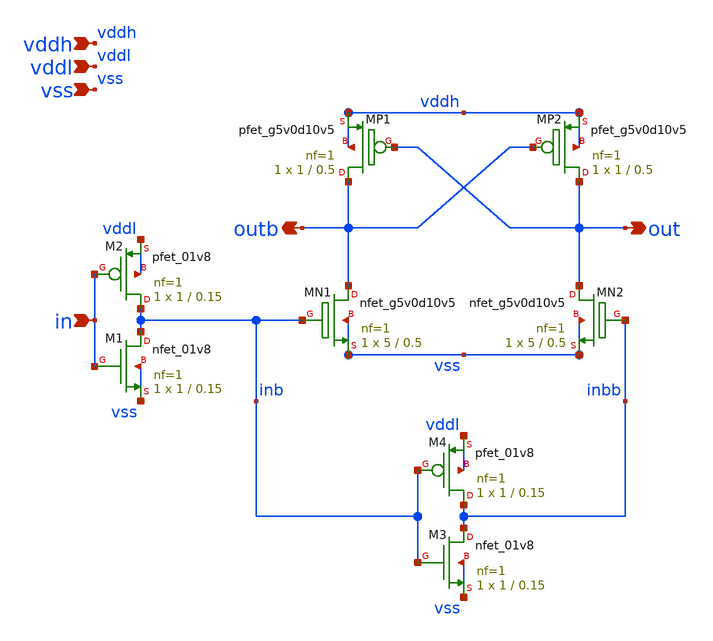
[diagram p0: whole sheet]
** sch_path: level_shifters/ls_conv.sch
**.subckt ls_conv vddh vss vddl in out outb
*.ipin vddh
*.ipin vss
*.ipin vddl
*.ipin in
*.opin out
*.opin outb
XMN1 outb inb vss vss sky130_fd_pr__nfet_g5v0d10v5 L=0.5 W=5 nf=1 ad='int((nf+1)/2) * W/nf * 0.29' as='int((nf+2)/2) * W/nf * 0.29'
+ pd='2*int((nf+1)/2) * (W/nf + 0.29)' ps='2*int((nf+2)/2) * (W/nf + 0.29)' nrd='0.29 / W' nrs='0.29 / W'
+ sa=0 sb=0 sd=0 mult=1 m=1
XMN2 out inbb vss vss sky130_fd_pr__nfet_g5v0d10v5 L=0.5 W=5 nf=1 ad='int((nf+1)/2) * W/nf * 0.29' as='int((nf+2)/2) * W/nf * 0.29'
+ pd='2*int((nf+1)/2) * (W/nf + 0.29)' ps='2*int((nf+2)/2) * (W/nf + 0.29)' nrd='0.29 / W' nrs='0.29 / W'
+ sa=0 sb=0 sd=0 mult=1 m=1
XMP1 outb out vddh vddh sky130_fd_pr__pfet_g5v0d10v5 L=0.5 W=1 nf=1 ad='int((nf+1)/2) * W/nf * 0.29'
+ as='int((nf+2)/2) * W/nf * 0.29' pd='2*int((nf+1)/2) * (W/nf + 0.29)' ps='2*int((nf+2)/2) * (W/nf + 0.29)'
+ nrd='0.29 / W' nrs='0.29 / W' sa=0 sb=0 sd=0 mult=1 m=1
XMP2 out outb vddh vddh sky130_fd_pr__pfet_g5v0d10v5 L=0.5 W=1 nf=1 ad='int((nf+1)/2) * W/nf * 0.29'
+ as='int((nf+2)/2) * W/nf * 0.29' pd='2*int((nf+1)/2) * (W/nf + 0.29)' ps='2*int((nf+2)/2) * (W/nf + 0.29)'
+ nrd='0.29 / W' nrs='0.29 / W' sa=0 sb=0 sd=0 mult=1 m=1
XM1 inb in vss vss sky130_fd_pr__nfet_01v8 L=0.15 W=1 nf=1 ad='int((nf+1)/2) * W/nf * 0.29' as='int((nf+2)/2) * W/nf * 0.29'
+ pd='2*int((nf+1)/2) * (W/nf + 0.29)' ps='2*int((nf+2)/2) * (W/nf + 0.29)' nrd='0.29 / W' nrs='0.29 / W'
+ sa=0 sb=0 sd=0 mult=1 m=1
XM2 inb in vddl vddl sky130_fd_pr__pfet_01v8 L=0.15 W=1 nf=1 ad='int((nf+1)/2) * W/nf * 0.29' as='int((nf+2)/2) * W/nf * 0.29'
+ pd='2*int((nf+1)/2) * (W/nf + 0.29)' ps='2*int((nf+2)/2) * (W/nf + 0.29)' nrd='0.29 / W' nrs='0.29 / W'
+ sa=0 sb=0 sd=0 mult=1 m=1
XM3 inbb inb vss vss sky130_fd_pr__nfet_01v8 L=0.15 W=1 nf=1 ad='int((nf+1)/2) * W/nf * 0.29' as='int((nf+2)/2) * W/nf * 0.29'
+ pd='2*int((nf+1)/2) * (W/nf + 0.29)' ps='2*int((nf+2)/2) * (W/nf + 0.29)' nrd='0.29 / W' nrs='0.29 / W'
+ sa=0 sb=0 sd=0 mult=1 m=1
XM4 inbb inb vddl vddl sky130_fd_pr__pfet_01v8 L=0.15 W=1 nf=1 ad='int((nf+1)/2) * W/nf * 0.29' as='int((nf+2)/2) * W/nf * 0.29'
+ pd='2*int((nf+1)/2) * (W/nf + 0.29)' ps='2*int((nf+2)/2) * (W/nf + 0.29)' nrd='0.29 / W' nrs='0.29 / W'
+ sa=0 sb=0 sd=0 mult=1 m=1
**.ends
.end
